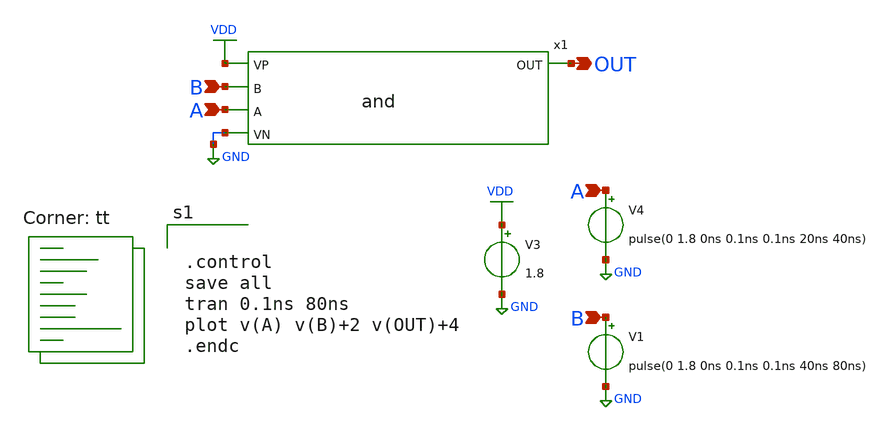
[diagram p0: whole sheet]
** sch_path: basic_cell/and/xschem/tb_xschem_and.sch
**.subckt tb_xschem_and A B A B OUT
*.ipin A
*.ipin B
*.ipin A
*.ipin B
*.opin OUT
V3 VDD GND 1.8
V4 A GND pulse(0 1.8 0ns 0.1ns 0.1ns 20ns 40ns)
V1 B GND pulse(0 1.8 0ns 0.1ns 0.1ns 40ns 80ns)
x1 VDD OUT B A GND and
**** begin user architecture code
.lib $::SKYWATER_MODELS/sky130.lib.spice tt


.control
save all
tran 0.1ns 80ns
plot v(A) v(B)+2 v(OUT)+4
.endc


**** end user architecture code
**.ends

* expanding   symbol:  and.sym # of pins=5
** sym_path: basic_cell/and/xschem/and.sym
** sch_path: basic_cell/and/xschem/and.sch
.subckt and VP OUT B A VN
*.ipin VP
*.ipin B
*.ipin A
*.ipin VN
*.opin OUT
x1 VP net1 B A VN nand
x2 VP net1 OUT VN inverter
.ends


* expanding   symbol:  /foss/designs/APIC_Mux_DFF/basic_cell/single_cell/nand/nand.sym # of pins=5
** sym_path: basic_cell/single_cell/nand/nand.sym
** sch_path: basic_cell/single_cell/nand/nand.sch
.subckt nand VP OUT B A VN
*.opin OUT
*.ipin A
*.ipin B
*.ipin VN
*.ipin VP
XM4 OUT A net1 VN sky130_fd_pr__nfet_01v8 L=0.15 W=1 nf=1 ad='int((nf+1)/2) * W/nf * 0.29' as='int((nf+2)/2) * W/nf * 0.29'
+ pd='2*int((nf+1)/2) * (W/nf + 0.29)' ps='2*int((nf+2)/2) * (W/nf + 0.29)' nrd='0.29 / W' nrs='0.29 / W'
+ sa=0 sb=0 sd=0 mult=1 m=1
XM3 net1 B VN VN sky130_fd_pr__nfet_01v8 L=0.15 W=1 nf=1 ad='int((nf+1)/2) * W/nf * 0.29' as='int((nf+2)/2) * W/nf * 0.29'
+ pd='2*int((nf+1)/2) * (W/nf + 0.29)' ps='2*int((nf+2)/2) * (W/nf + 0.29)' nrd='0.29 / W' nrs='0.29 / W'
+ sa=0 sb=0 sd=0 mult=1 m=1
XM1 OUT A VP VP sky130_fd_pr__pfet_01v8 L=0.15 W=3 nf=1 ad='int((nf+1)/2) * W/nf * 0.29' as='int((nf+2)/2) * W/nf * 0.29'
+ pd='2*int((nf+1)/2) * (W/nf + 0.29)' ps='2*int((nf+2)/2) * (W/nf + 0.29)' nrd='0.29 / W' nrs='0.29 / W'
+ sa=0 sb=0 sd=0 mult=1 m=1
XM2 OUT B VP VP sky130_fd_pr__pfet_01v8 L=0.15 W=3 nf=1 ad='int((nf+1)/2) * W/nf * 0.29' as='int((nf+2)/2) * W/nf * 0.29'
+ pd='2*int((nf+1)/2) * (W/nf + 0.29)' ps='2*int((nf+2)/2) * (W/nf + 0.29)' nrd='0.29 / W' nrs='0.29 / W'
+ sa=0 sb=0 sd=0 mult=1 m=1
.ends


* expanding   symbol:  /foss/designs/APIC_Mux_DFF/basic_cell/single_cell/inverter/inverter.sym # of
*+ pins=4
** sym_path: basic_cell/single_cell/inverter/inverter.sym
** sch_path: basic_cell/single_cell/inverter/inverter.sch
.subckt inverter VP A OUT VN
*.ipin A
*.ipin VP
*.ipin VN
*.opin OUT
XM1 OUT A VP VP sky130_fd_pr__pfet_01v8 L=0.15 W=3 nf=1 ad='int((nf+1)/2) * W/nf * 0.29' as='int((nf+2)/2) * W/nf * 0.29'
+ pd='2*int((nf+1)/2) * (W/nf + 0.29)' ps='2*int((nf+2)/2) * (W/nf + 0.29)' nrd='0.29 / W' nrs='0.29 / W'
+ sa=0 sb=0 sd=0 mult=1 m=1
XM2 OUT A VN VN sky130_fd_pr__nfet_01v8 L=0.15 W=1 nf=1 ad='int((nf+1)/2) * W/nf * 0.29' as='int((nf+2)/2) * W/nf * 0.29'
+ pd='2*int((nf+1)/2) * (W/nf + 0.29)' ps='2*int((nf+2)/2) * (W/nf + 0.29)' nrd='0.29 / W' nrs='0.29 / W'
+ sa=0 sb=0 sd=0 mult=1 m=1
.ends

.GLOBAL VDD
.GLOBAL GND
.end
